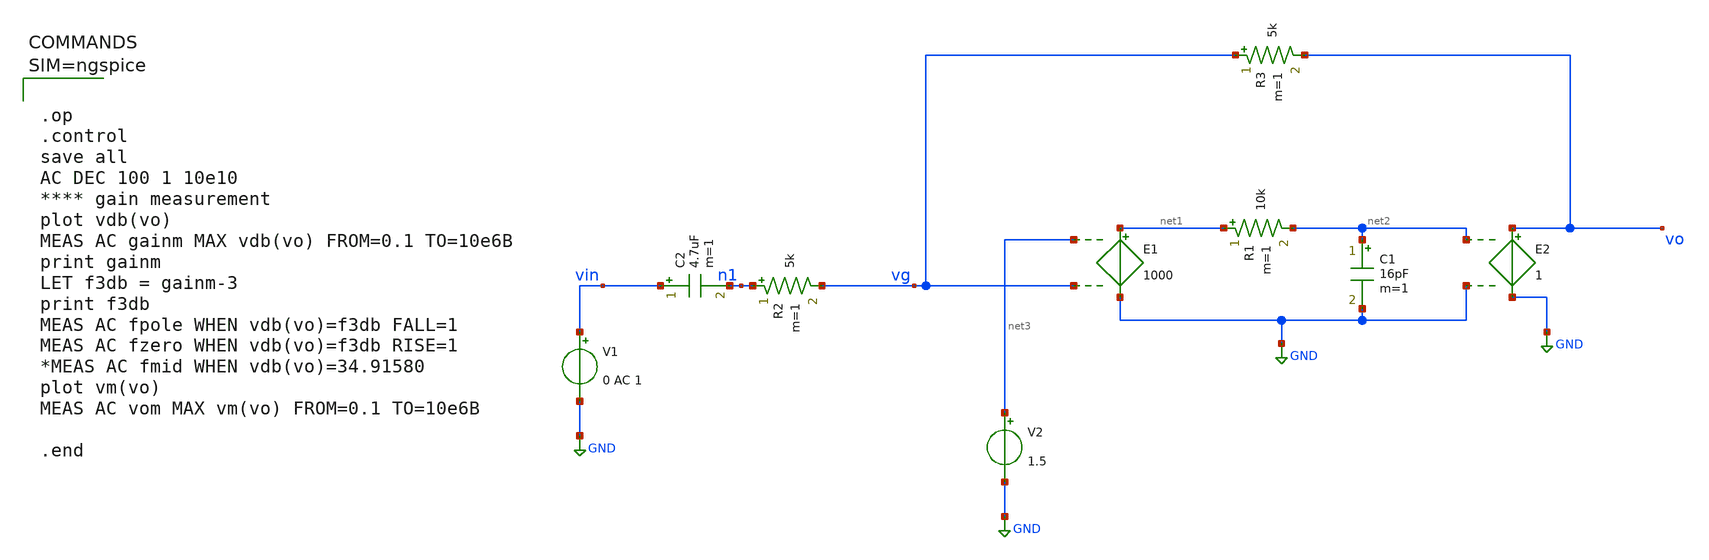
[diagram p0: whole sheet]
** sch_path: xschem_eg/2_vcvs.sch
**.subckt 2_vcvs
E1 net1 GND net3 vg 1000
E2 vo GND net2 GND 1
R1 net1 net2 10k m=1
C1 net2 GND 16pF m=1
V1 vin GND 0 AC 1
V2 net3 GND 1.5
R2 n1 vg 5k m=1
R3 vg vo 5k m=1
C2 vin n1 4.7uF m=1
**** begin user architecture code



.op
.control
save all
AC DEC 100 1 10e10
**** gain measurement
plot vdb(vo)
MEAS AC gainm MAX vdb(vo) FROM=0.1 TO=10e6B
print gainm
LET f3db = gainm-3
print f3db
MEAS AC fpole WHEN vdb(vo)=f3db FALL=1
MEAS AC fzero WHEN vdb(vo)=f3db RISE=1
*MEAS AC fmid WHEN vdb(vo)=34.91580
plot vm(vo)
MEAS AC vom MAX vm(vo) FROM=0.1 TO=10e6B

.end



**** end user architecture code
**.ends
.GLOBAL GND
.end
